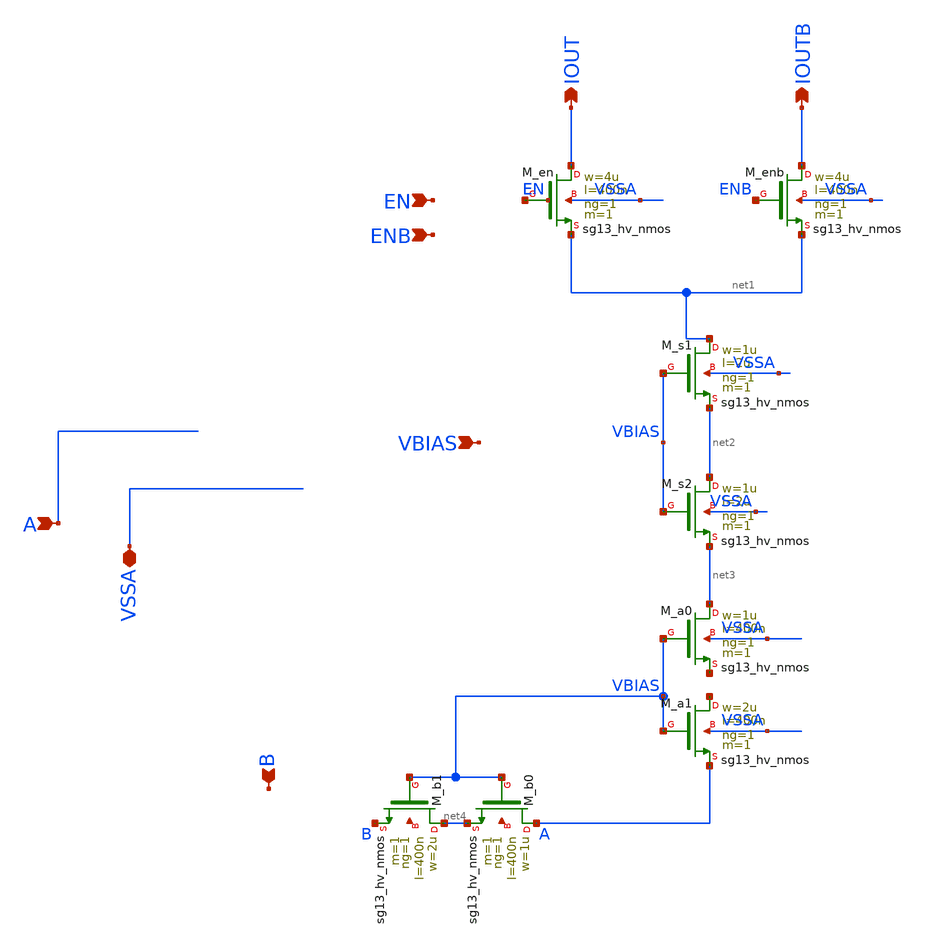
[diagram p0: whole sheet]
** sch_path: SplitterCell.sch
**.subckt SplitterCell EN ENB VBIAS A B IOUT IOUTB VSSA
*.ipin EN
*.ipin ENB
*.ipin VBIAS
*.ipin A
*.ipin B
*.opin IOUT
*.opin IOUTB
*.iopin VSSA
XM_en IOUT net5 net1 VSSA sg13_hv_nmos w=4u l=400n ng=1 m=1 mm_ok=1
XM_enb IOUTB ENB net1 VSSA sg13_hv_nmos w=4u l=400n ng=1 m=1 mm_ok=1
XM_s1 net1 VBIAS net2 VSSA sg13_hv_nmos w=1u l=2u ng=1 m=1 mm_ok=1
XM_s2 net2 VBIAS net3 VSSA sg13_hv_nmos w=1u l=2u ng=1 m=1 mm_ok=1
XM_a0 net3 VBIAS net6 VSSA sg13_hv_nmos w=1u l=400n ng=1 m=1 mm_ok=1
XM_a1 net7 VBIAS A VSSA sg13_hv_nmos w=2u l=400n ng=1 m=1 mm_ok=1
XM_b0 A VBIAS net4 net8 sg13_hv_nmos w=1u l=400n ng=1 m=1 mm_ok=1
XM_b1 net4 VBIAS B net9 sg13_hv_nmos w=2u l=400n ng=1 m=1 mm_ok=1
**.ends
.end
